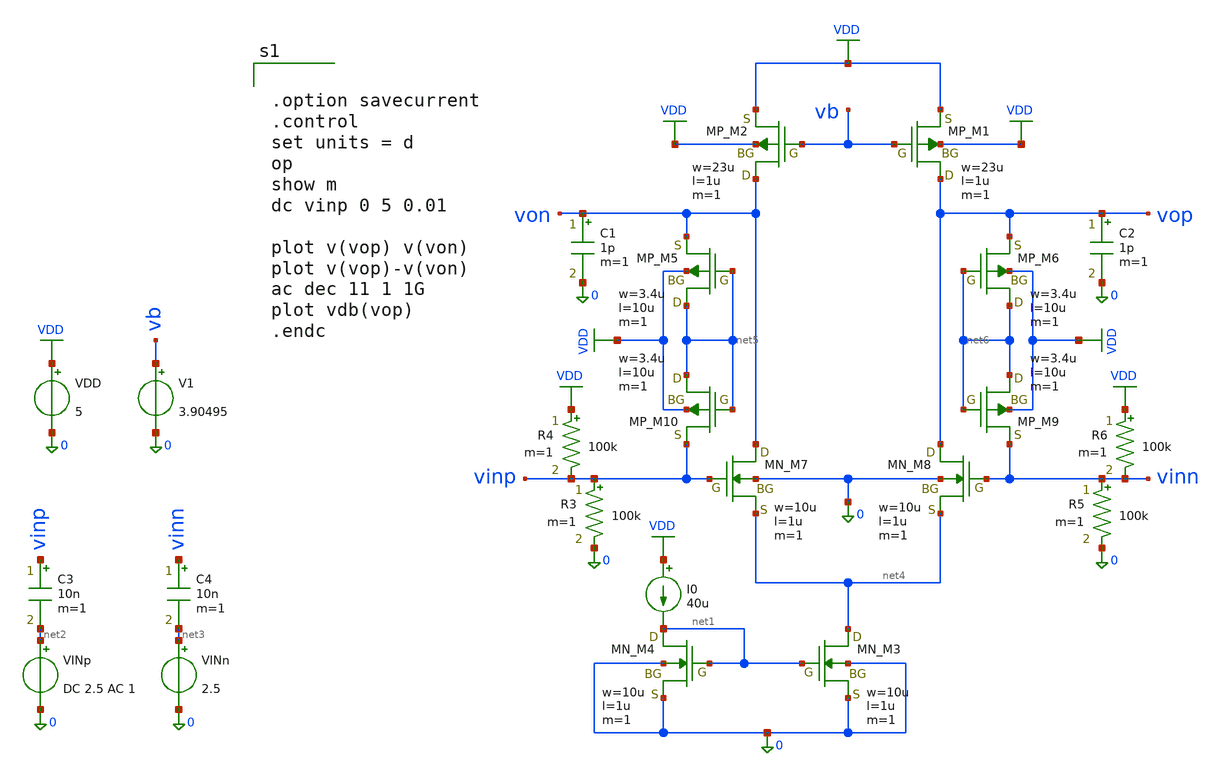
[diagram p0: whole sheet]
** sch_path: member_project/JJY_Receiver/Masahiro/jjy_recv/diff_amp/diff_amp_nin_shortl.sch
**.subckt diff_amp_nin_shortl
VDD VDD 0 5
VINp net2 0 DC 2.5 AC 1
I0 VDD net1 40u
C1 von 0 1p m=1
V1 vb 0 3.90495
XM1 vop vb VDD VDD PMOS w=23u l=1u as=0 ad=0 ps=0 pd=0 nrd=0 nrs=0 m=1
XM2 von vb VDD VDD PMOS w=23u l=1u as=0 ad=0 ps=0 pd=0 nrd=0 nrs=0 m=1
XM3 net4 net1 0 0 NMOS w=10u l=1u as=0 ad=0 ps=0 pd=0 nrd=0 nrs=0 m=1
XM4 net1 net1 0 0 NMOS w=10u l=1u as=0 ad=0 ps=0 pd=0 nrd=0 nrs=0 m=1
C2 vop 0 1p m=1
VINn net3 0 2.5
XM7 von vinp net4 0 NMOS w=10u l=1u as=0 ad=0 ps=0 pd=0 nrd=0 nrs=0 m=1
XM8 vop vinn net4 0 NMOS w=10u l=1u as=0 ad=0 ps=0 pd=0 nrd=0 nrs=0 m=1
C3 vinp net2 10n m=1
C4 vinn net3 10n m=1
XM5 net5 net5 von VDD PMOS w=3.4u l=10u as=0 ad=0 ps=0 pd=0 nrd=0 nrs=0 m=1
XM10 net5 net5 vinp VDD PMOS w=3.4u l=10u as=0 ad=0 ps=0 pd=0 nrd=0 nrs=0 m=1
XM6 net6 net6 vop VDD PMOS w=3.4u l=10u as=0 ad=0 ps=0 pd=0 nrd=0 nrs=0 m=1
XM9 net6 net6 vinn VDD PMOS w=3.4u l=10u as=0 ad=0 ps=0 pd=0 nrd=0 nrs=0 m=1
R3 vinp 0 100k m=1
R4 VDD vinp 100k m=1
R5 vinn 0 100k m=1
R6 VDD vinn 100k m=1
**** begin user architecture code
 .include $::LIB/ip62_models


.option savecurrent
.control
set units = d
op
show m
dc vinp 0 5 0.01

plot v(vop) v(von)
plot v(vop)-v(von)
ac dec 11 1 1G
plot vdb(vop)
.endc


**** end user architecture code
**.ends
.GLOBAL VDD
.end
